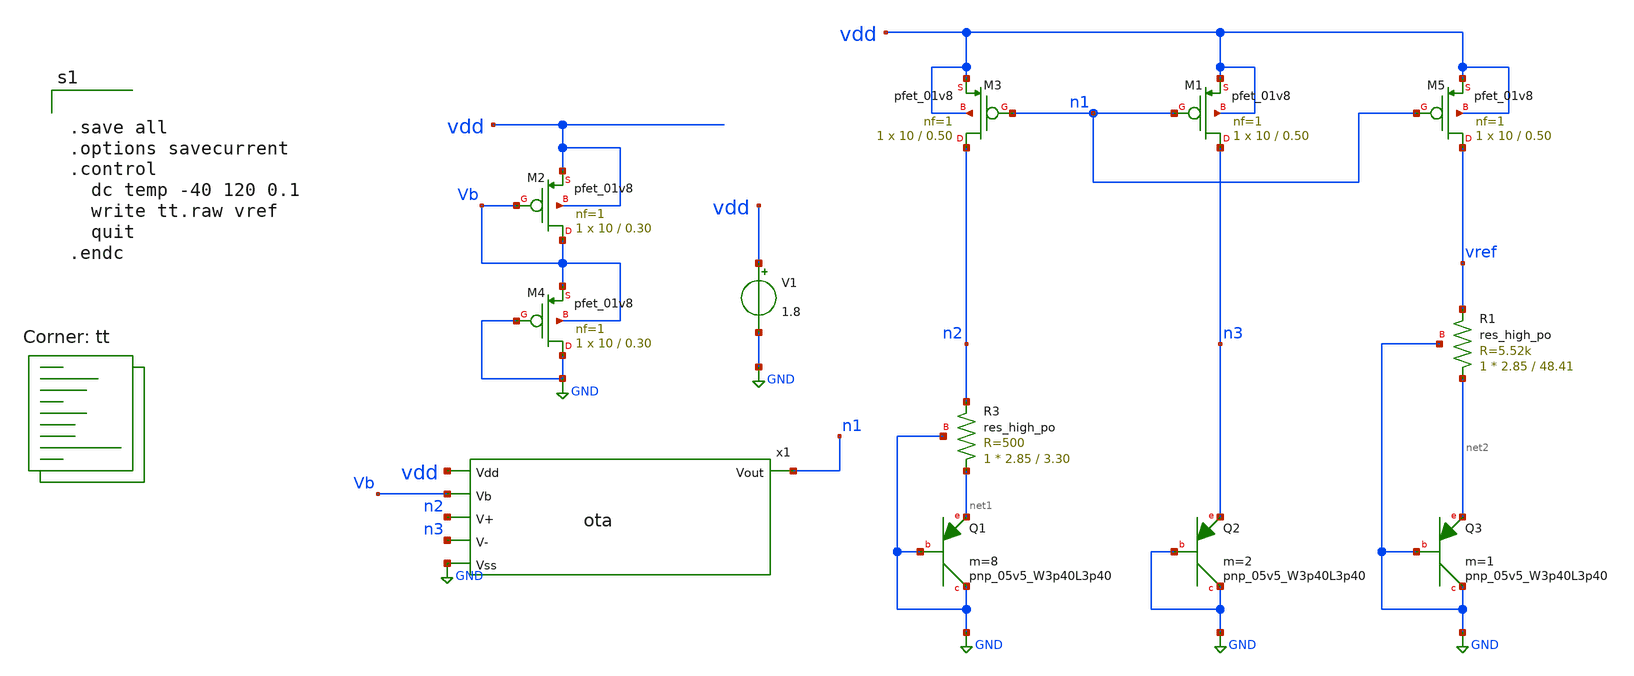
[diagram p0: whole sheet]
** sch_path: Bandgap/Bandgap.sch
**.subckt Bandgap
V1 vdd GND 1.8
XM1 n3 n1 vdd vdd sky130_fd_pr__pfet_01v8 L=0.50 W=10 nf=1 ad='int((1 + 1)/2) * 10 / 1 * 0.29' as='int((1 + 2)/2) * 10 / 1 * 0.29'
+ pd='2*int((1 + 1)/2) * (10 / 1 + 0.29)' ps='2*int((1 + 2)/2) * (10 / 1 + 0.29)' nrd='0.29 / 10 ' nrs='0.29 / 10 '
+ sa=0 sb=0 sd=0 mult=1 m=1
XM3 n2 n1 vdd vdd sky130_fd_pr__pfet_01v8 L=0.50 W=10 nf=1 ad='int((1 + 1)/2) * 10 / 1 * 0.29' as='int((1 + 2)/2) * 10 / 1 * 0.29'
+ pd='2*int((1 + 1)/2) * (10 / 1 + 0.29)' ps='2*int((1 + 2)/2) * (10 / 1 + 0.29)' nrd='0.29 / 10 ' nrs='0.29 / 10 '
+ sa=0 sb=0 sd=0 mult=1 m=1
XQ1 GND GND net1 sky130_fd_pr__pnp_05v5_W3p40L3p40 m=8
XQ2 GND GND n3 sky130_fd_pr__pnp_05v5_W3p40L3p40 m=2
XM2 Vb Vb vdd vdd sky130_fd_pr__pfet_01v8 L=0.30 W=10 nf=1 ad='int((1 + 1)/2) * 10 / 1 * 0.29' as='int((1 + 2)/2) * 10 / 1 * 0.29'
+ pd='2*int((1 + 1)/2) * (10 / 1 + 0.29)' ps='2*int((1 + 2)/2) * (10 / 1 + 0.29)' nrd='0.29 / 10 ' nrs='0.29 / 10 '
+ sa=0 sb=0 sd=0 mult=1 m=1
XM4 GND GND Vb Vb sky130_fd_pr__pfet_01v8 L=0.30 W=10 nf=1 ad='int((1 + 1)/2) * 10 / 1 * 0.29' as='int((1 + 2)/2) * 10 / 1 * 0.29'
+ pd='2*int((1 + 1)/2) * (10 / 1 + 0.29)' ps='2*int((1 + 2)/2) * (10 / 1 + 0.29)' nrd='0.29 / 10 ' nrs='0.29 / 10 '
+ sa=0 sb=0 sd=0 mult=1 m=1
XM5 vref n1 vdd vdd sky130_fd_pr__pfet_01v8 L=0.50 W=10 nf=1 ad='int((1 + 1)/2) * 10 / 1 * 0.29' as='int((1 + 2)/2) * 10 / 1 * 0.29'
+ pd='2*int((1 + 1)/2) * (10 / 1 + 0.29)' ps='2*int((1 + 2)/2) * (10 / 1 + 0.29)' nrd='0.29 / 10 ' nrs='0.29 / 10 '
+ sa=0 sb=0 sd=0 mult=1 m=1
XQ3 GND GND net2 sky130_fd_pr__pnp_05v5_W3p40L3p40 m=1
x1 vdd Vb n2 n3 n1 GND ota
XR3 net1 n2 GND sky130_fd_pr__res_high_po W=2.85 L=3.30 mult=1 m=1
XR1 net2 vref GND sky130_fd_pr__res_high_po W=2.85 L=48.41 mult=1 m=1
**** begin user architecture code


.save all
.options savecurrent
.control
  dc temp -40 120 0.1
  write tt.raw vref
  quit
.endc


.lib $::SKYWATER_MODELS/sky130.lib.spice tt
**** end user architecture code
**.ends

* expanding   symbol:  ota.sym # of pins=6
** sym_path: Bandgap/ota.sym
** sch_path: Bandgap/ota.sch
.subckt ota Vdd Vb V+ V- Vout Vss
*.ipin Vdd
*.opin Vout
*.ipin V+
*.ipin V-
*.ipin Vss
*.ipin Vb
XM1 net1 Vb Vdd Vdd sky130_fd_pr__pfet_01v8 L=0.50 W=16 nf=1 ad='int((1 + 1)/2) * 16 / 1 * 0.29' as='int((1 + 2)/2) * 16 / 1 * 0.29'
+ pd='2*int((1 + 1)/2) * (16 / 1 + 0.29)' ps='2*int((1 + 2)/2) * (16 / 1 + 0.29)' nrd='0.29 / 16 ' nrs='0.29 / 16 '
+ sa=0 sb=0 sd=0 mult=1 m=1
XM2 net2 V+ net1 net1 sky130_fd_pr__pfet_01v8 L=0.50 W=16 nf=1 ad='int((1 + 1)/2) * 16 / 1 * 0.29' as='int((1 + 2)/2) * 16 / 1 * 0.29'
+ pd='2*int((1 + 1)/2) * (16 / 1 + 0.29)' ps='2*int((1 + 2)/2) * (16 / 1 + 0.29)' nrd='0.29 / 16 ' nrs='0.29 / 16 '
+ sa=0 sb=0 sd=0 mult=1 m=1
XM3 Vout V- net1 net1 sky130_fd_pr__pfet_01v8 L=0.50 W=16 nf=1 ad='int((1 + 1)/2) * 16 / 1 * 0.29' as='int((1 + 2)/2) * 16 / 1 * 0.29'
+ pd='2*int((1 + 1)/2) * (16 / 1 + 0.29)' ps='2*int((1 + 2)/2) * (16 / 1 + 0.29)' nrd='0.29 / 16 ' nrs='0.29 / 16 '
+ sa=0 sb=0 sd=0 mult=1 m=1
XM4 Vout net2 Vss Vss sky130_fd_pr__nfet_01v8 L=1 W=10 nf=1 ad='int((1 + 1)/2) * 10 / 1 * 0.29' as='int((1 + 2)/2) * 10 / 1 * 0.29'
+ pd='2*int((1 + 1)/2) * (10 / 1 + 0.29)' ps='2*int((1 + 2)/2) * (10 / 1 + 0.29)' nrd='0.29 / 10 ' nrs='0.29 / 10 '
+ sa=0 sb=0 sd=0 mult=1 m=1
XM5 net2 net2 Vss Vss sky130_fd_pr__nfet_01v8 L=1 W=10 nf=1 ad='int((1 + 1)/2) * 10 / 1 * 0.29' as='int((1 + 2)/2) * 10 / 1 * 0.29'
+ pd='2*int((1 + 1)/2) * (10 / 1 + 0.29)' ps='2*int((1 + 2)/2) * (10 / 1 + 0.29)' nrd='0.29 / 10 ' nrs='0.29 / 10 '
+ sa=0 sb=0 sd=0 mult=1 m=1
.ends

.GLOBAL GND
.end
